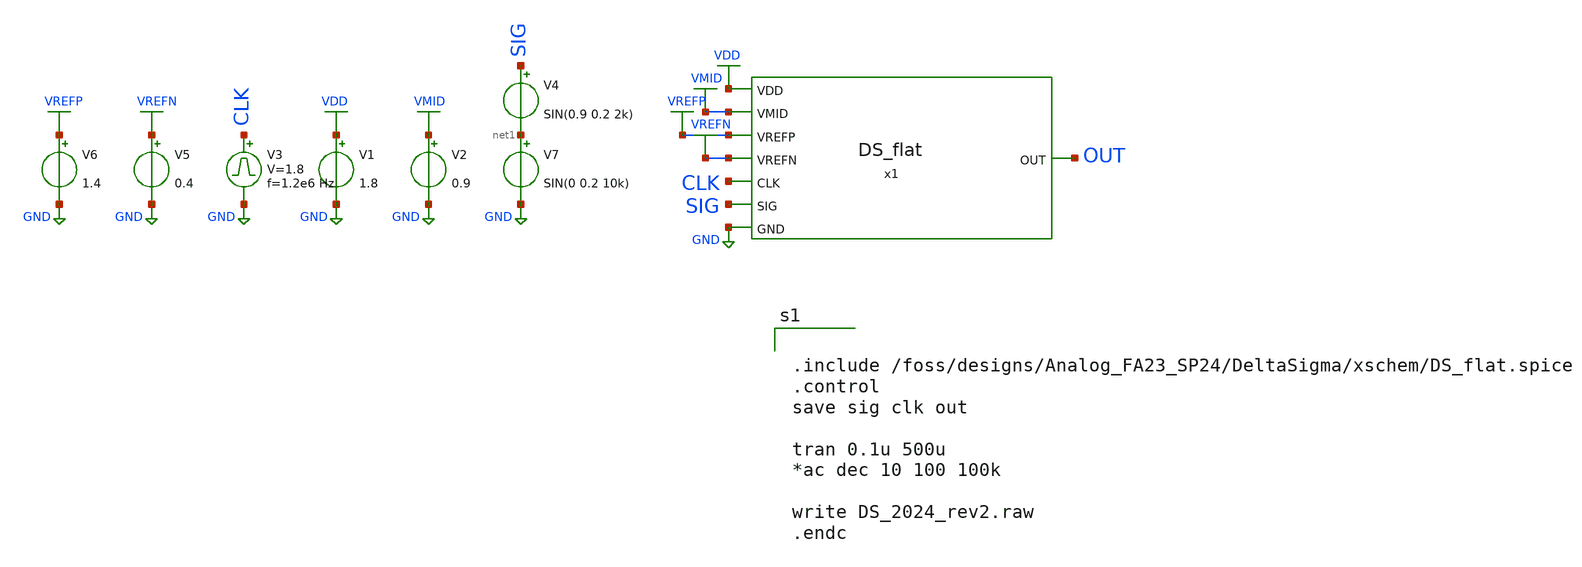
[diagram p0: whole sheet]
** sch_path: DeltaSigma/xschem/DS_2024_Bench_ext.sch
.lib $::SKYWATER_MODELS/sky130.lib.spice tt
.include $::SKYWATER_STDCELLS/sky130_fd_sc_hd.spice

**.subckt DS_2024_Bench_ext
V1 VDD GND 1.8
V2 VMID GND 0.9
V3 CLK GND pulse 0 1.8 '0.495/ 1.2e6 ' '0.01/1.2e6 ' '0.01/1.2e6 ' '0.49/1.2e6 ' '1/1.2e6 '
V5 VREFN GND 0.4
V6 VREFP GND 1.4
x1 GND VREFP VREFN SIG VMID OUT CLK VDD DS_flat
V4 SIG net1 SIN(0.9 0.2 2k)
V7 net1 GND SIN(0 0.2 10k)
**** begin user architecture code


.include /foss/designs/Analog_FA23_SP24/DeltaSigma/xschem/DS_flat.spice
.control
save sig clk out

tran 0.1u 500u
*ac dec 10 100 100k

write DS_2024_rev2.raw
.endc


**** end user architecture code
**.ends
.GLOBAL VDD
.GLOBAL GND
.GLOBAL VMID
.GLOBAL VREFN
.GLOBAL VREFP
.end
